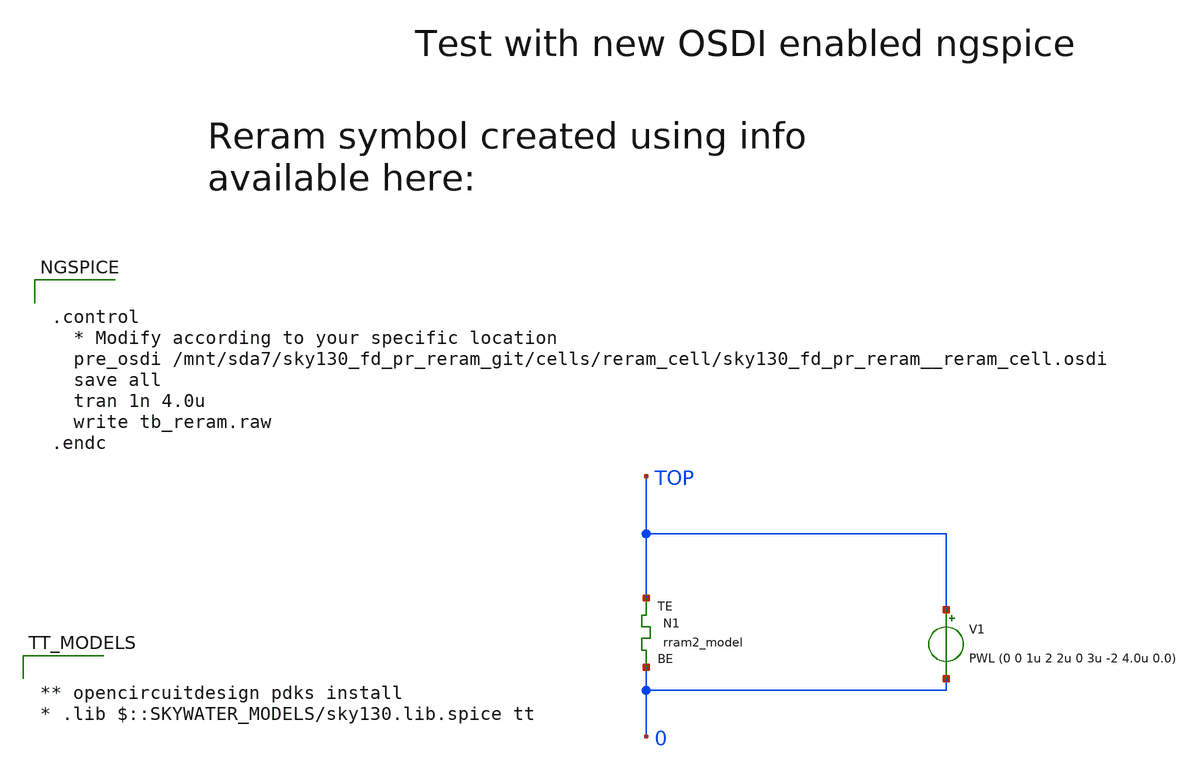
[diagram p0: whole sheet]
** sch_path: sky130_tests/tb_reram.sch
* Copyright 2021 Stefan Frederik Schippers
* Licensed under the Apache License, Version 2.0 (the "License");
* you may not use this file except in compliance with the License.
* You may obtain a copy of the License at
* https://www.apache.org/licenses/LICENSE-2.0
* Unless required by applicable law or agreed to in writing, software
* distributed under the License is distributed on an "AS IS" BASIS,
* WITHOUT WARRANTIES OR CONDITIONS OF ANY KIND, either express or implied.
* See the License for the specific language governing permissions and
* limitations under the License.
**.subckt tb_reram
N1 0 TOP rram2_model m=1
V1 TOP 0 PWL (0 0 1u 2 2u 0 3u -2 4.0u 0.0)
**** begin user architecture code


.control
  * Modify according to your specific location
  pre_osdi /mnt/sda7/sky130_fd_pr_reram_git/cells/reram_cell/sky130_fd_pr_reram__reram_cell.osdi
  save all
  tran 1n 4.0u
  write tb_reram.raw
.endc




** opencircuitdesign pdks install
* .lib $::SKYWATER_MODELS/sky130.lib.spice tt

**** end user architecture code
**.ends
**** begin user architecture code
.model rram2_model rram2 rram2_params.scs
**** end user architecture code
.end
